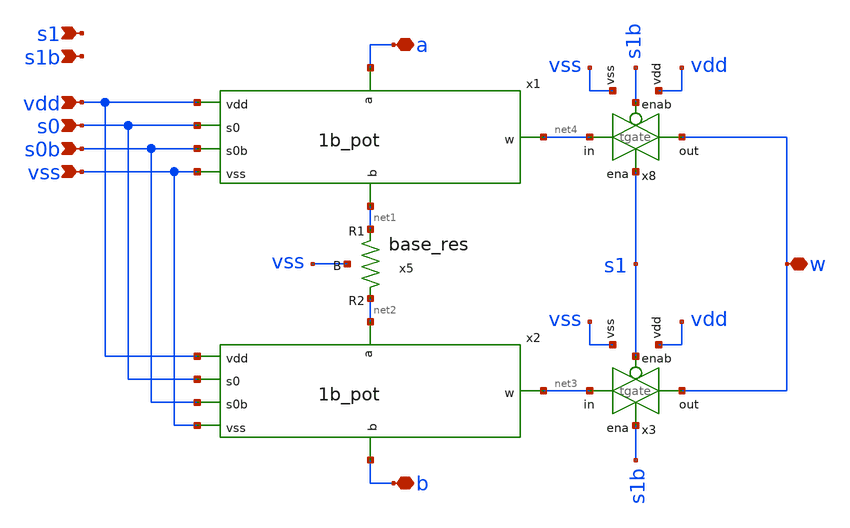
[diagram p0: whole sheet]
** sch_path: xschem/2b_pot.sch
**.subckt 2b_pot s0 s0b s1 vss vdd a w b s1b
*.ipin s0
*.ipin s0b
*.ipin s1
*.ipin vss
*.ipin vdd
*.iopin a
*.iopin w
*.iopin b
*.ipin s1b
x1 vdd a net4 s0b s0 net1 vss 1b_pot
x2 vdd net2 net3 s0b s0 b vss 1b_pot
x5 net1 net2 vss base_res
x8 vdd s1b net4 w s1 vss tgate
x3 vdd s1 net3 w s1b vss tgate
**.ends

* expanding   symbol:  xschem/1b_pot.sym # of pins=7
** sym_path: xschem/1b_pot.sym
** sch_path: xschem/1b_pot.sch
.subckt 1b_pot vdd a w s0b s0 b vss
*.ipin s0
*.ipin s0b
*.ipin vdd
*.ipin vss
*.ipin a
*.ipin b
*.opin w
x1 a b vss base_res
x2 vdd s0b a w s0 vss tgate
x3 vdd s0 b w s0b vss tgate
.ends


* expanding   symbol:  xschem/base_res.sym # of pins=3
** sym_path: xschem/base_res.sym
** sch_path: xschem/base_res.sch
.subckt base_res R1 R2 B
*.iopin R1
*.iopin R2
*.iopin B
XR2 R2 R1 B sky130_fd_pr__res_high_po_2p85 L=0.57 mult=1 m=1
.ends


* expanding   symbol:  xschem/tgate.sym # of pins=6
** sym_path: xschem/tgate.sym
** sch_path: xschem/tgate.sch
.subckt tgate vdd enab in out ena vss
*.ipin enab
*.ipin ena
*.ipin in
*.opin out
*.iopin vdd
*.iopin vss
XMn out ena in vss sky130_fd_pr__nfet_g5v0d10v5 L=0.5 W=80 nf=4 ad='int((nf+1)/2) * W/nf * 0.29' as='int((nf+2)/2) * W/nf * 0.29'
+ pd='2*int((nf+1)/2) * (W/nf + 0.29)' ps='2*int((nf+2)/2) * (W/nf + 0.29)' nrd='0.29 / W' nrs='0.29 / W'
+ sa=0 sb=0 sd=0 mult=1 m=1
XMp out enab in vdd sky130_fd_pr__pfet_g5v0d10v5 L=0.5 W=80 nf=4 ad='int((nf+1)/2) * W/nf * 0.29' as='int((nf+2)/2) * W/nf * 0.29'
+ pd='2*int((nf+1)/2) * (W/nf + 0.29)' ps='2*int((nf+2)/2) * (W/nf + 0.29)' nrd='0.29 / W' nrs='0.29 / W'
+ sa=0 sb=0 sd=0 mult=1 m=1
.ends

.end
